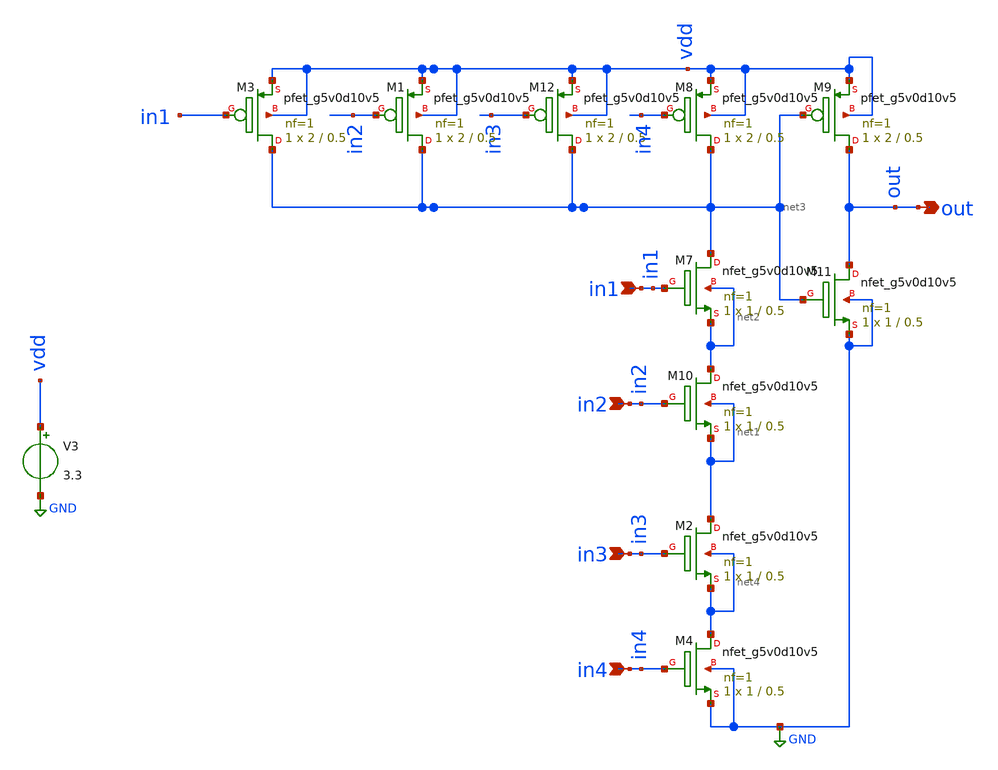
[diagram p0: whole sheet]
** sch_path: xschem/FDC/four_input_and.sch
**.subckt four_input_and in1 in2 out in3 in4
*.ipin in1
*.ipin in2
*.opin out
*.ipin in3
*.ipin in4
XM7 net3 in1 net2 net2 sky130_fd_pr__nfet_g5v0d10v5 L=0.5 W=1 nf=1 ad='int((nf+1)/2) * W/nf * 0.29' as='int((nf+2)/2) * W/nf * 0.29'
+ pd='2*int((nf+1)/2) * (W/nf + 0.29)' ps='2*int((nf+2)/2) * (W/nf + 0.29)' nrd='0.29 / W' nrs='0.29 / W'
+ sa=0 sb=0 sd=0 mult=1 m=1
XM8 net3 in4 vdd vdd sky130_fd_pr__pfet_g5v0d10v5 L=0.5 W=2 nf=1 ad='int((nf+1)/2) * W/nf * 0.29' as='int((nf+2)/2) * W/nf * 0.29'
+ pd='2*int((nf+1)/2) * (W/nf + 0.29)' ps='2*int((nf+2)/2) * (W/nf + 0.29)' nrd='0.29 / W' nrs='0.29 / W'
+ sa=0 sb=0 sd=0 mult=1 m=1
XM9 out net3 vdd vdd sky130_fd_pr__pfet_g5v0d10v5 L=0.5 W=2 nf=1 ad='int((nf+1)/2) * W/nf * 0.29' as='int((nf+2)/2) * W/nf * 0.29'
+ pd='2*int((nf+1)/2) * (W/nf + 0.29)' ps='2*int((nf+2)/2) * (W/nf + 0.29)' nrd='0.29 / W' nrs='0.29 / W'
+ sa=0 sb=0 sd=0 mult=1 m=1
XM10 net2 in2 net1 net1 sky130_fd_pr__nfet_g5v0d10v5 L=0.5 W=1 nf=1 ad='int((nf+1)/2) * W/nf * 0.29'
+ as='int((nf+2)/2) * W/nf * 0.29' pd='2*int((nf+1)/2) * (W/nf + 0.29)' ps='2*int((nf+2)/2) * (W/nf + 0.29)'
+ nrd='0.29 / W' nrs='0.29 / W' sa=0 sb=0 sd=0 mult=1 m=1
XM11 out net3 GND GND sky130_fd_pr__nfet_g5v0d10v5 L=0.5 W=1 nf=1 ad='int((nf+1)/2) * W/nf * 0.29' as='int((nf+2)/2) * W/nf * 0.29'
+ pd='2*int((nf+1)/2) * (W/nf + 0.29)' ps='2*int((nf+2)/2) * (W/nf + 0.29)' nrd='0.29 / W' nrs='0.29 / W'
+ sa=0 sb=0 sd=0 mult=1 m=1
XM12 net3 in3 vdd vdd sky130_fd_pr__pfet_g5v0d10v5 L=0.5 W=2 nf=1 ad='int((nf+1)/2) * W/nf * 0.29' as='int((nf+2)/2) * W/nf * 0.29'
+ pd='2*int((nf+1)/2) * (W/nf + 0.29)' ps='2*int((nf+2)/2) * (W/nf + 0.29)' nrd='0.29 / W' nrs='0.29 / W'
+ sa=0 sb=0 sd=0 mult=1 m=1
V3 vdd GND 3.3
XM1 net3 in2 vdd vdd sky130_fd_pr__pfet_g5v0d10v5 L=0.5 W=2 nf=1 ad='int((nf+1)/2) * W/nf * 0.29' as='int((nf+2)/2) * W/nf * 0.29'
+ pd='2*int((nf+1)/2) * (W/nf + 0.29)' ps='2*int((nf+2)/2) * (W/nf + 0.29)' nrd='0.29 / W' nrs='0.29 / W'
+ sa=0 sb=0 sd=0 mult=1 m=1
XM2 net1 in3 net4 net4 sky130_fd_pr__nfet_g5v0d10v5 L=0.5 W=1 nf=1 ad='int((nf+1)/2) * W/nf * 0.29' as='int((nf+2)/2) * W/nf * 0.29'
+ pd='2*int((nf+1)/2) * (W/nf + 0.29)' ps='2*int((nf+2)/2) * (W/nf + 0.29)' nrd='0.29 / W' nrs='0.29 / W'
+ sa=0 sb=0 sd=0 mult=1 m=1
XM3 net3 in1 vdd vdd sky130_fd_pr__pfet_g5v0d10v5 L=0.5 W=2 nf=1 ad='int((nf+1)/2) * W/nf * 0.29' as='int((nf+2)/2) * W/nf * 0.29'
+ pd='2*int((nf+1)/2) * (W/nf + 0.29)' ps='2*int((nf+2)/2) * (W/nf + 0.29)' nrd='0.29 / W' nrs='0.29 / W'
+ sa=0 sb=0 sd=0 mult=1 m=1
XM4 net4 in4 GND GND sky130_fd_pr__nfet_g5v0d10v5 L=0.5 W=1 nf=1 ad='int((nf+1)/2) * W/nf * 0.29' as='int((nf+2)/2) * W/nf * 0.29'
+ pd='2*int((nf+1)/2) * (W/nf + 0.29)' ps='2*int((nf+2)/2) * (W/nf + 0.29)' nrd='0.29 / W' nrs='0.29 / W'
+ sa=0 sb=0 sd=0 mult=1 m=1
**.ends
.GLOBAL GND
.end
